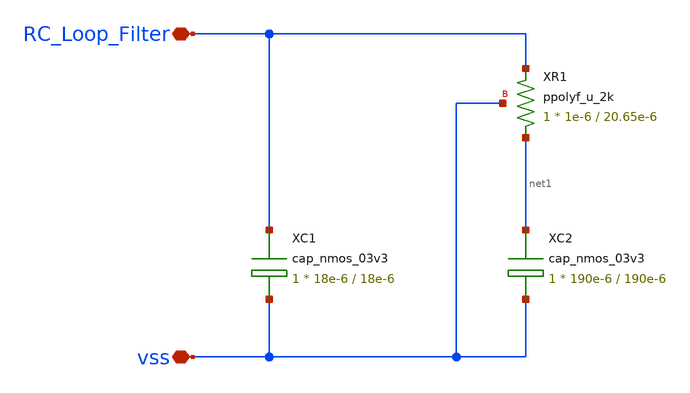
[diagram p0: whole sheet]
** sch_path: PLL/analog/schematics/RC_Varactor.sch
**.subckt RC_Varactor RC_Loop_Filter vss
*.iopin RC_Loop_Filter
*.iopin vss
XC1 RC_Loop_Filter vss cap_nmos_03v3 c_width=18e-6 c_length=18e-6 m=1
XC2 net1 vss cap_nmos_03v3 c_width=190e-6 c_length=190e-6 m=1
XR1 net1 RC_Loop_Filter vss ppolyf_u_2k r_width=1e-6 r_length=20.65e-6 m=1
**.ends
.end
